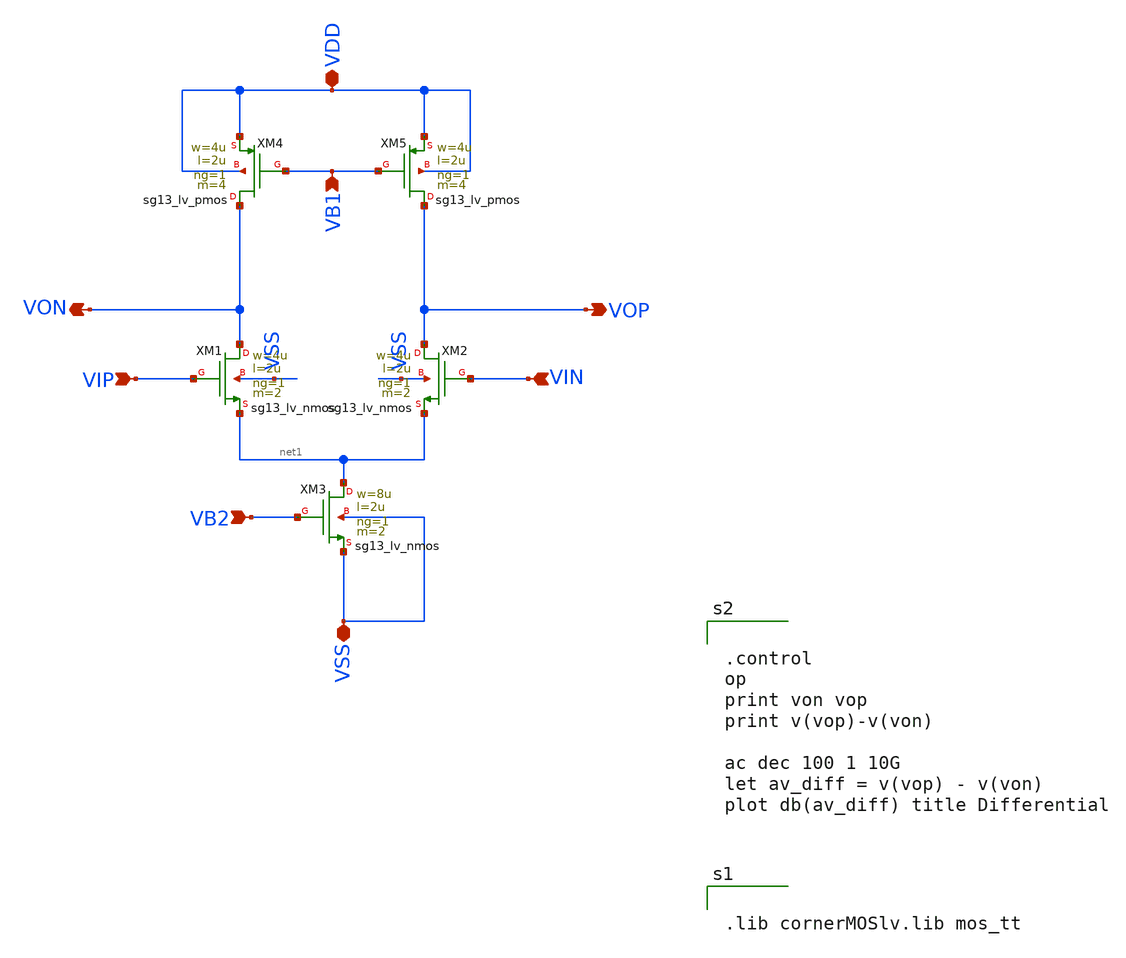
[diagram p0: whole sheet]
** sch_path: BTDay4-Ex/diff_cs_load.sch
**.subckt diff_cs_load VIN VIP VON VOP VB2 VDD VSS VB1
*.ipin VIN
*.ipin VIP
*.opin VON
*.opin VOP
*.ipin VB2
*.iopin VDD
*.iopin VSS
*.ipin VB1
XXM1 VON VIP net1 VSS sg13_lv_nmos w=4u l=2u ng=1 m=2 mm_ok=1
XXM2 VOP VIN net1 VSS sg13_lv_nmos w=4u l=2u ng=1 m=2 mm_ok=1
XXM3 net1 VB2 VSS VSS sg13_lv_nmos w=8u l=2u ng=1 m=2 mm_ok=1
XXM4 VON VB1 VDD VDD sg13_lv_pmos w=4u l=2u ng=1 m=4 mm_ok=1
XXM5 VOP VB1 VDD VDD sg13_lv_pmos w=4u l=2u ng=1 m=4 mm_ok=1
**** begin user architecture code


.lib cornerMOSlv.lib mos_tt




.control
op
print von vop
print v(vop)-v(von)

ac dec 100 1 10G
let av_diff = v(vop) - v(von)
plot db(av_diff) title Differential

**** end user architecture code
**.ends
.end
